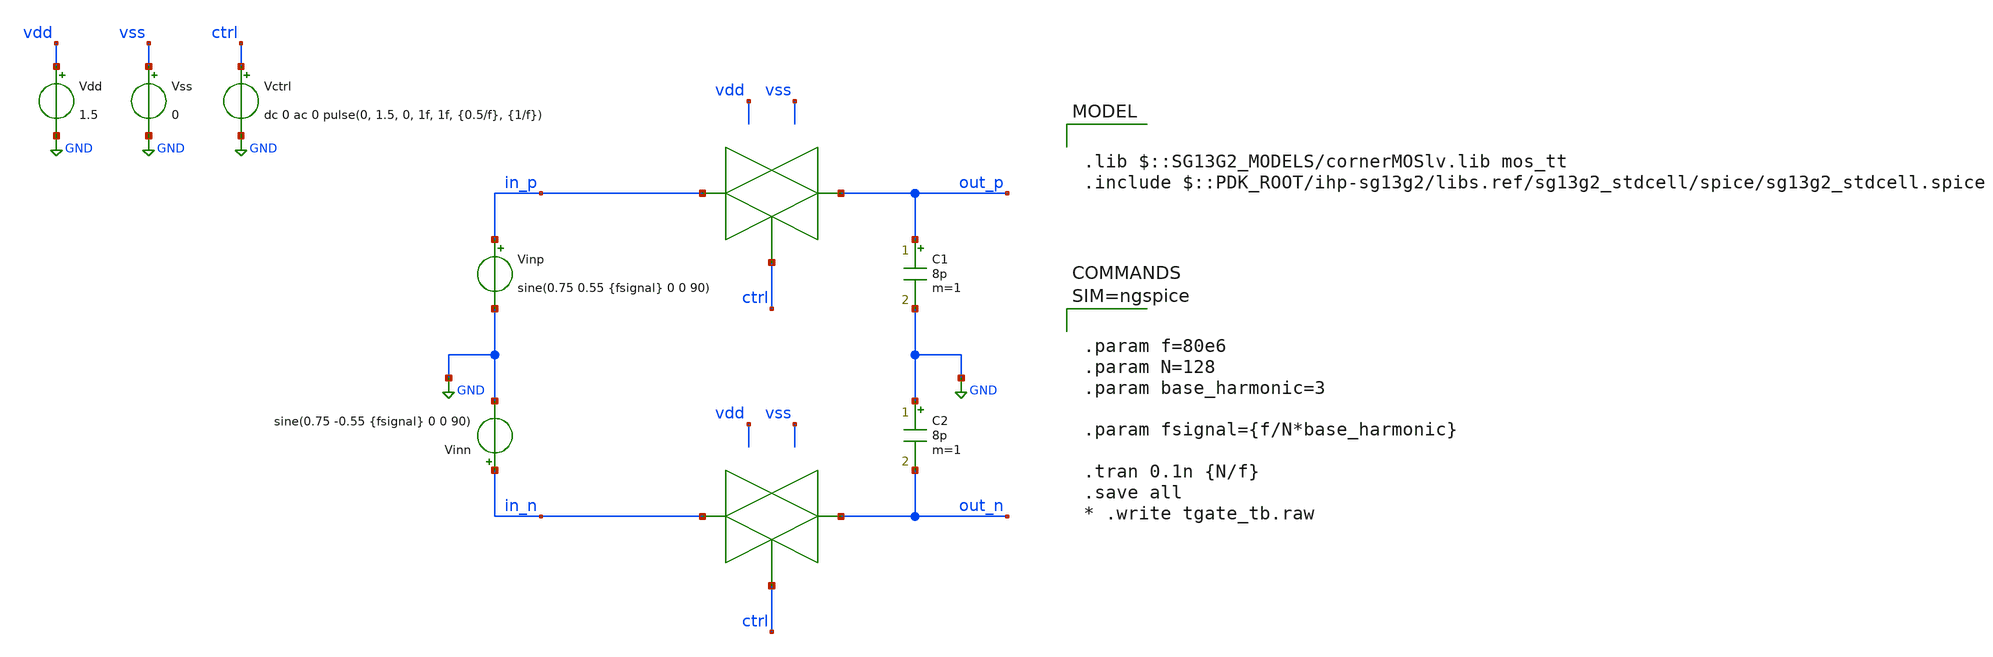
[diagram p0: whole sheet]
** sch_path: designs/tgate/tgate_tb.sch
**.subckt tgate_tb
Vdd vdd GND 1.5
Vss vss GND 0
C1 out_p GND 8p m=1
Vinp in_p GND sine(0.75 0.55 {fsignal} 0 0 90)
C2 GND out_n 8p m=1
Vinn in_n GND sine(0.75 -0.55 {fsignal} 0 0 90)
Vctrl ctrl GND dc 0 ac 0 pulse(0, 1.5, 0, 1f, 1f, {0.5/f}, {1/f})
**** begin user architecture code



.param f=80e6
.param N=128
.param base_harmonic=3

.param fsignal={f/N*base_harmonic}

.tran 0.1n {N/f}
.save all
* .write tgate_tb.raw




.lib $::SG13G2_MODELS/cornerMOSlv.lib mos_tt
.include $::PDK_ROOT/ihp-sg13g2/libs.ref/sg13g2_stdcell/spice/sg13g2_stdcell.spice

**** end user architecture code
**.ends
.GLOBAL GND
.end
